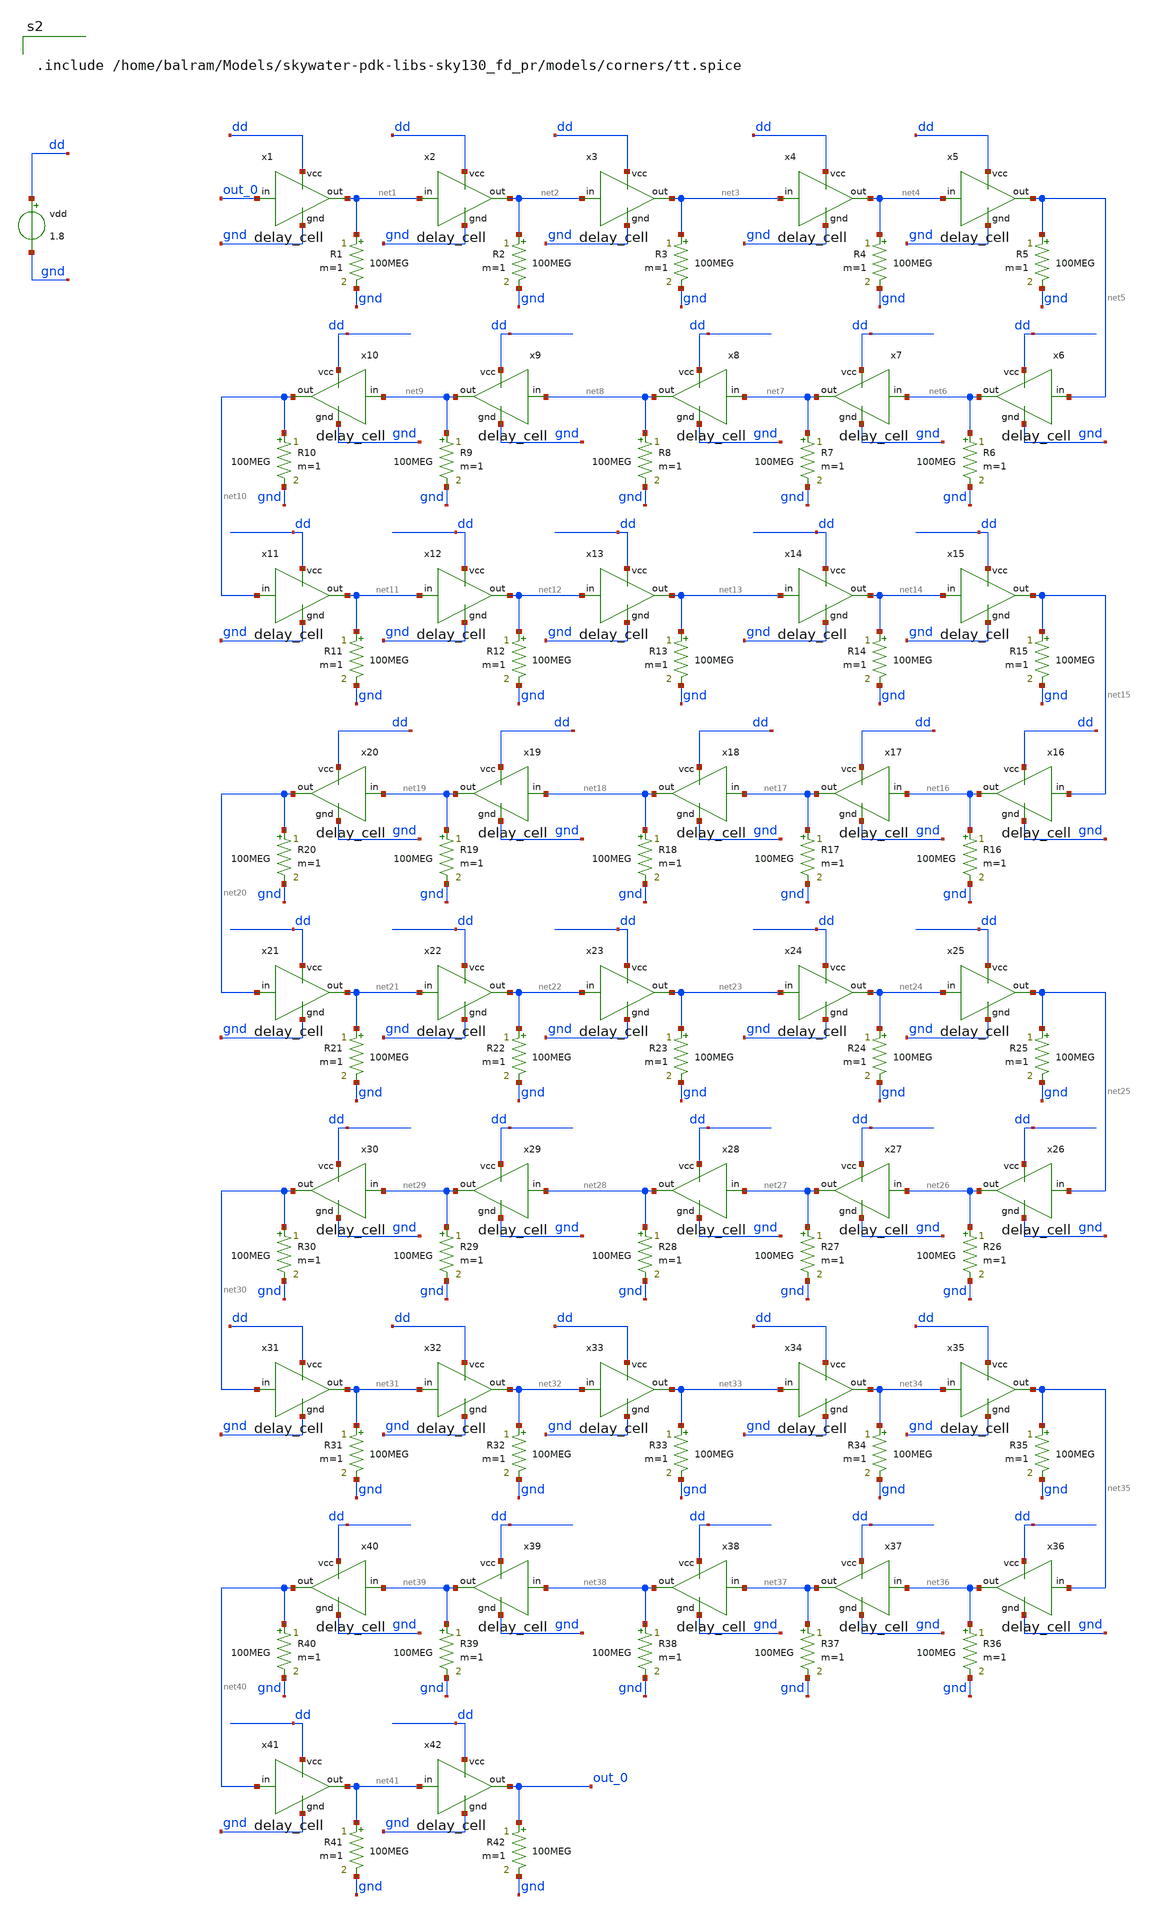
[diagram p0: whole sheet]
** sch_path: Oscillators/Ring-Oscillator/TB__oscillator.sch
**.subckt TB__oscillator
x1 dd out_0 net1 gnd delay_cell
vdd dd gnd 1.8
x2 dd net1 net2 gnd delay_cell
x3 dd net2 net3 gnd delay_cell
R1 net1 gnd 100MEG m=1
R2 net2 gnd 100MEG m=1
R3 net3 gnd 100MEG m=1
x4 dd net3 net4 gnd delay_cell
x5 dd net4 net5 gnd delay_cell
R4 net4 gnd 100MEG m=1
R5 net5 gnd 100MEG m=1
x6 dd net5 net6 gnd delay_cell
x7 dd net6 net7 gnd delay_cell
x8 dd net7 net8 gnd delay_cell
R6 net6 gnd 100MEG m=1
R7 net7 gnd 100MEG m=1
R8 net8 gnd 100MEG m=1
x9 dd net8 net9 gnd delay_cell
x10 dd net9 net10 gnd delay_cell
R9 net9 gnd 100MEG m=1
R10 net10 gnd 100MEG m=1
x11 dd net10 net11 gnd delay_cell
x12 dd net11 net12 gnd delay_cell
x13 dd net12 net13 gnd delay_cell
R11 net11 gnd 100MEG m=1
R12 net12 gnd 100MEG m=1
R13 net13 gnd 100MEG m=1
x14 dd net13 net14 gnd delay_cell
x15 dd net14 net15 gnd delay_cell
R14 net14 gnd 100MEG m=1
R15 net15 gnd 100MEG m=1
x16 dd net15 net16 gnd delay_cell
x17 dd net16 net17 gnd delay_cell
x18 dd net17 net18 gnd delay_cell
R16 net16 gnd 100MEG m=1
R17 net17 gnd 100MEG m=1
R18 net18 gnd 100MEG m=1
x19 dd net18 net19 gnd delay_cell
x20 dd net19 net20 gnd delay_cell
R19 net19 gnd 100MEG m=1
R20 net20 gnd 100MEG m=1
x21 dd net20 net21 gnd delay_cell
x22 dd net21 net22 gnd delay_cell
x23 dd net22 net23 gnd delay_cell
R21 net21 gnd 100MEG m=1
R22 net22 gnd 100MEG m=1
R23 net23 gnd 100MEG m=1
x24 dd net23 net24 gnd delay_cell
x25 dd net24 net25 gnd delay_cell
R24 net24 gnd 100MEG m=1
R25 net25 gnd 100MEG m=1
x26 dd net25 net26 gnd delay_cell
x27 dd net26 net27 gnd delay_cell
x28 dd net27 net28 gnd delay_cell
R26 net26 gnd 100MEG m=1
R27 net27 gnd 100MEG m=1
R28 net28 gnd 100MEG m=1
x29 dd net28 net29 gnd delay_cell
x30 dd net29 net30 gnd delay_cell
R29 net29 gnd 100MEG m=1
R30 net30 gnd 100MEG m=1
x31 dd net30 net31 gnd delay_cell
x32 dd net31 net32 gnd delay_cell
x33 dd net32 net33 gnd delay_cell
R31 net31 gnd 100MEG m=1
R32 net32 gnd 100MEG m=1
R33 net33 gnd 100MEG m=1
x34 dd net33 net34 gnd delay_cell
x35 dd net34 net35 gnd delay_cell
R34 net34 gnd 100MEG m=1
R35 net35 gnd 100MEG m=1
x36 dd net35 net36 gnd delay_cell
x37 dd net36 net37 gnd delay_cell
x38 dd net37 net38 gnd delay_cell
R36 net36 gnd 100MEG m=1
R37 net37 gnd 100MEG m=1
R38 net38 gnd 100MEG m=1
x39 dd net38 net39 gnd delay_cell
x40 dd net39 net40 gnd delay_cell
R39 net39 gnd 100MEG m=1
R40 net40 gnd 100MEG m=1
x41 dd net40 net41 gnd delay_cell
x42 dd net41 out_0 gnd delay_cell
R41 net41 gnd 100MEG m=1
R42 out_0 gnd 100MEG m=1
**** begin user architecture code


.include /home/balram/Models/skywater-pdk-libs-sky130_fd_pr/models/corners/tt.spice


**** end user architecture code
**.ends

* expanding   symbol:  delay_cell.sym # of pins=4
** sym_path: Oscillators/Ring-Oscillator/delay_cell.sym
** sch_path: Oscillators/Ring-Oscillator/delay_cell.sch
.subckt delay_cell vcc in out gnd
*.ipin vcc
*.ipin gnd
*.ipin in
*.opin out
XM1 out in gnd gnd sky130_fd_pr__nfet_01v8_lvt L=0.15 W=0.45 nf=1 ad='int((1 + 1)/2) * 0.45 / 1 * 0.29'
+ as='int((1 + 2)/2) * 0.45 / 1 * 0.29' pd='2*int((1 + 1)/2) * (0.45 / 1 + 0.29)' ps='2*int((1 + 2)/2) * (0.45 / 1 + 0.29)'
+ nrd='0.29 / 0.45 ' nrs='0.29 / 0.45 ' sa=0 sb=0 sd=0 mult=1 m=1
XM10 out in vcc vcc sky130_fd_pr__pfet_01v8_lvt L=0.35 W=0.45 nf=1 ad='int((1 + 1)/2) * 0.45 / 1 * 0.29'
+ as='int((1 + 2)/2) * 0.45 / 1 * 0.29' pd='2*int((1 + 1)/2) * (0.45 / 1 + 0.29)' ps='2*int((1 + 2)/2) * (0.45 / 1 + 0.29)'
+ nrd='0.29 / 0.45 ' nrs='0.29 / 0.45 ' sa=0 sb=0 sd=0 mult=1 m=1
.ends

.end
